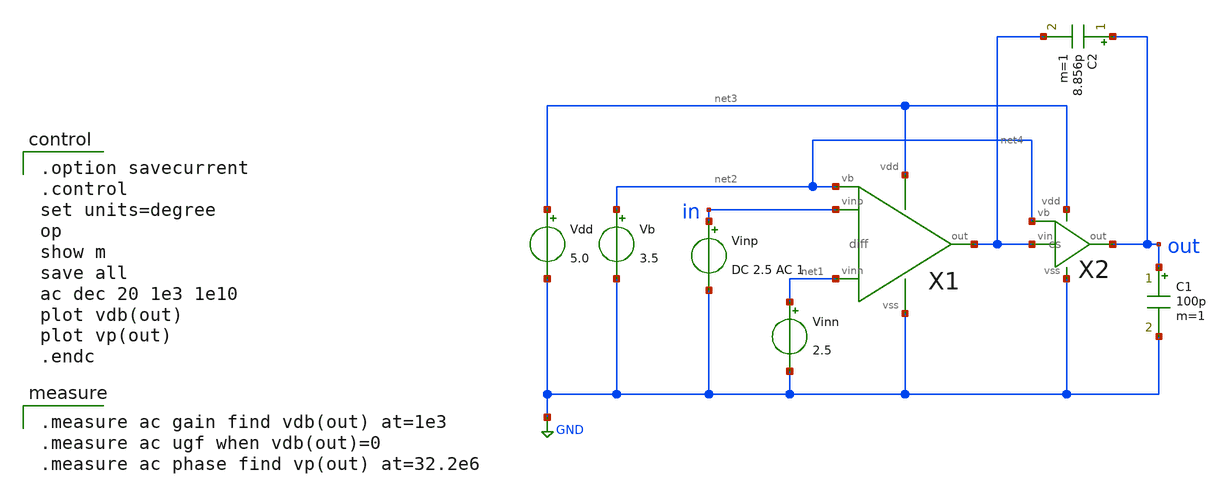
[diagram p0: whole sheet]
** sch_path: OpenSUSI-TR10/opamp/2stage_cc_ac.sch
**.subckt 2stage_cc_ac
Vdd net3 GND 5.0
Vb net2 GND 3.5
Vinn net1 GND 2.5
Vinp in GND DC 2.5 AC 1
X1 in net1 net4 net3 GND net2 diff
X2 net4 net2 out net3 GND cs
C1 out GND 100p m=1
C2 out net4 8.856p m=1
**** begin user architecture code

.option savecurrent
.control
set units=degree
op
show m
save all
ac dec 20 1e3 1e10
plot vdb(out)
plot vp(out)
.endc


.measure ac gain find vdb(out) at=1e3
.measure ac ugf when vdb(out)=0
.measure ac phase find vp(out) at=32.2e6

 .include $::LIB/ip62_models
**** end user architecture code
**.ends

* expanding   symbol:  diff.sym # of pins=6
** sym_path: diff.sym
** sch_path: diff.sch
.subckt diff vinp vinn out vdd vss vb
*.ipin vinn
*.ipin vinp
*.ipin vb
*.opin out
*.iopin vdd
*.iopin vss
M5 net2 vb vdd vdd pmos L=2u W=40u m=1
M1 net1 vinn net2 net2 pmos L=2u W=200u m=1
M2 out vinp net2 net2 pmos L=2u W=200u m=1
M3 net1 net1 vss vss nmos L=2u W=10u m=1
M4 out net1 vss vss nmos L=2u W=10u m=1
.ends


* expanding   symbol:  cs.sym # of pins=5
** sym_path: cs.sym
** sch_path: cs.sch
.subckt cs vin vb out vdd vss
*.ipin vb
*.ipin vin
*.opin out
*.iopin vss
*.iopin vdd
XM6 out vb vdd vdd PMOS w=270u l=1u as=0 ad=0 ps=0 pd=0 nrd=0 nrs=0 m=1
XM7 out vin vss vss NMOS w=90u l=1u as=0 ad=0 ps=0 pd=0 nrd=0 nrs=0 m=1
.ends

.GLOBAL GND
.end
